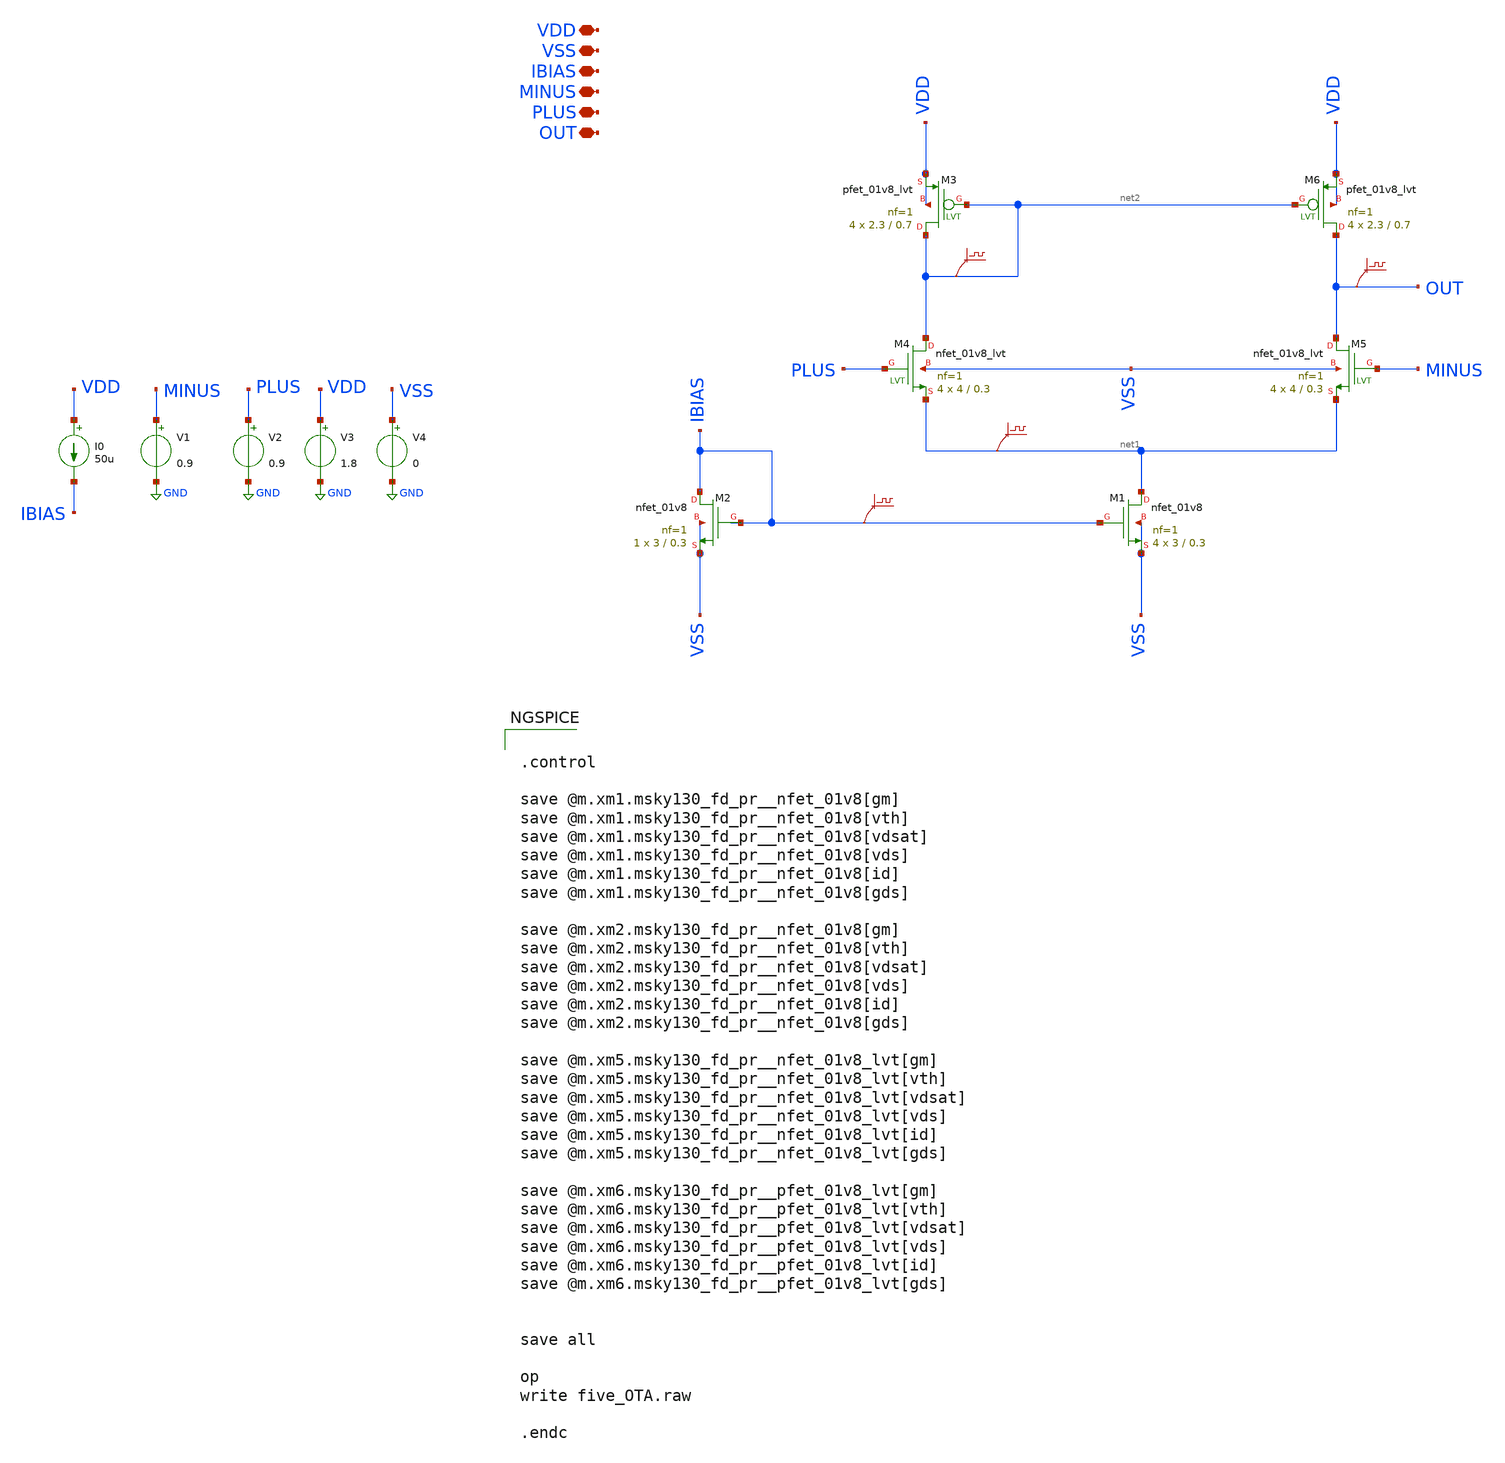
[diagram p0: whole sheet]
** sch_path: five_OTA/five_OTA.sch
**.subckt five_OTA VDD VSS IBIAS MINUS PLUS OUT
*.iopin VDD
*.iopin VSS
*.iopin IBIAS
*.iopin MINUS
*.iopin PLUS
*.iopin OUT
XM4 net2 PLUS net1 VSS sky130_fd_pr__nfet_01v8_lvt L=0.3 W=4 nf=1 ad='int((nf+1)/2) * W/nf * 0.29' as='int((nf+2)/2) * W/nf * 0.29'
+ pd='2*int((nf+1)/2) * (W/nf + 0.29)' ps='2*int((nf+2)/2) * (W/nf + 0.29)' nrd='0.29 / W' nrs='0.29 / W'
+ sa=0 sb=0 sd=0 mult=4 m=4
XM5 OUT MINUS net1 VSS sky130_fd_pr__nfet_01v8_lvt L=0.3 W=4 nf=1 ad='int((nf+1)/2) * W/nf * 0.29' as='int((nf+2)/2) * W/nf * 0.29'
+ pd='2*int((nf+1)/2) * (W/nf + 0.29)' ps='2*int((nf+2)/2) * (W/nf + 0.29)' nrd='0.29 / W' nrs='0.29 / W'
+ sa=0 sb=0 sd=0 mult=4 m=4
XM1 net1 IBIAS VSS VSS sky130_fd_pr__nfet_01v8 L=0.3 W=3 nf=1 ad='int((nf+1)/2) * W/nf * 0.29' as='int((nf+2)/2) * W/nf * 0.29'
+ pd='2*int((nf+1)/2) * (W/nf + 0.29)' ps='2*int((nf+2)/2) * (W/nf + 0.29)' nrd='0.29 / W' nrs='0.29 / W'
+ sa=0 sb=0 sd=0 mult=4 m=4
XM2 IBIAS IBIAS VSS VSS sky130_fd_pr__nfet_01v8 L=0.3 W=3 nf=1 ad='int((nf+1)/2) * W/nf * 0.29' as='int((nf+2)/2) * W/nf * 0.29'
+ pd='2*int((nf+1)/2) * (W/nf + 0.29)' ps='2*int((nf+2)/2) * (W/nf + 0.29)' nrd='0.29 / W' nrs='0.29 / W'
+ sa=0 sb=0 sd=0 mult=1 m=1
XM3 net2 net2 VDD VDD sky130_fd_pr__pfet_01v8_lvt L=0.7 W=2.3 nf=1 ad='int((nf+1)/2) * W/nf * 0.29' as='int((nf+2)/2) * W/nf * 0.29'
+ pd='2*int((nf+1)/2) * (W/nf + 0.29)' ps='2*int((nf+2)/2) * (W/nf + 0.29)' nrd='0.29 / W' nrs='0.29 / W'
+ sa=0 sb=0 sd=0 mult=4 m=4
XM6 OUT net2 VDD VDD sky130_fd_pr__pfet_01v8_lvt L=0.7 W=2.3 nf=1 ad='int((nf+1)/2) * W/nf * 0.29' as='int((nf+2)/2) * W/nf * 0.29'
+ pd='2*int((nf+1)/2) * (W/nf + 0.29)' ps='2*int((nf+2)/2) * (W/nf + 0.29)' nrd='0.29 / W' nrs='0.29 / W'
+ sa=0 sb=0 sd=0 mult=4 m=4
V1 MINUS GND 0.9
V2 PLUS GND 0.9
V3 VDD GND 1.8
V4 VSS GND 0
I0 VDD IBIAS 50u
.save v(net2)
.save v(ibias)
.save v(net1)
.save v(out)
**** begin user architecture code


.control

save @m.xm1.msky130_fd_pr__nfet_01v8[gm]
save @m.xm1.msky130_fd_pr__nfet_01v8[vth]
save @m.xm1.msky130_fd_pr__nfet_01v8[vdsat]
save @m.xm1.msky130_fd_pr__nfet_01v8[vds]
save @m.xm1.msky130_fd_pr__nfet_01v8[id]
save @m.xm1.msky130_fd_pr__nfet_01v8[gds]

save @m.xm2.msky130_fd_pr__nfet_01v8[gm]
save @m.xm2.msky130_fd_pr__nfet_01v8[vth]
save @m.xm2.msky130_fd_pr__nfet_01v8[vdsat]
save @m.xm2.msky130_fd_pr__nfet_01v8[vds]
save @m.xm2.msky130_fd_pr__nfet_01v8[id]
save @m.xm2.msky130_fd_pr__nfet_01v8[gds]

save @m.xm5.msky130_fd_pr__nfet_01v8_lvt[gm]
save @m.xm5.msky130_fd_pr__nfet_01v8_lvt[vth]
save @m.xm5.msky130_fd_pr__nfet_01v8_lvt[vdsat]
save @m.xm5.msky130_fd_pr__nfet_01v8_lvt[vds]
save @m.xm5.msky130_fd_pr__nfet_01v8_lvt[id]
save @m.xm5.msky130_fd_pr__nfet_01v8_lvt[gds]

save @m.xm6.msky130_fd_pr__pfet_01v8_lvt[gm]
save @m.xm6.msky130_fd_pr__pfet_01v8_lvt[vth]
save @m.xm6.msky130_fd_pr__pfet_01v8_lvt[vdsat]
save @m.xm6.msky130_fd_pr__pfet_01v8_lvt[vds]
save @m.xm6.msky130_fd_pr__pfet_01v8_lvt[id]
save @m.xm6.msky130_fd_pr__pfet_01v8_lvt[gds]


save all

op
write five_OTA.raw

.endc



** opencircuitdesign pdks install
.lib $::SKYWATER_MODELS/sky130.lib.spice tt


**** end user architecture code
**.ends
.GLOBAL GND
.end
